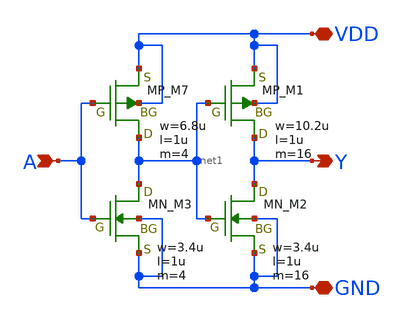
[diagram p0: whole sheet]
** sch_path: libs.tech/xschem/TR-1um_5_stdcell/BUF_X16.sch
**.subckt BUF_X16 A Y VDD GND
*.ipin A
*.opin Y
*.iopin VDD
*.iopin GND
XM7 net1 A VDD VDD PMOS w=6.8u l=1u nrd=0 nrs=0 m=4
XM1 Y net1 VDD VDD PMOS w=10.2u l=1u nrd=0 nrs=0 m=16
XM3 net1 A GND GND NMOS w=3.4u l=1u nrd=0 nrs=0 m=4
XM2 Y net1 GND GND NMOS w=3.4u l=1u nrd=0 nrs=0 m=16
**.ends
.end
